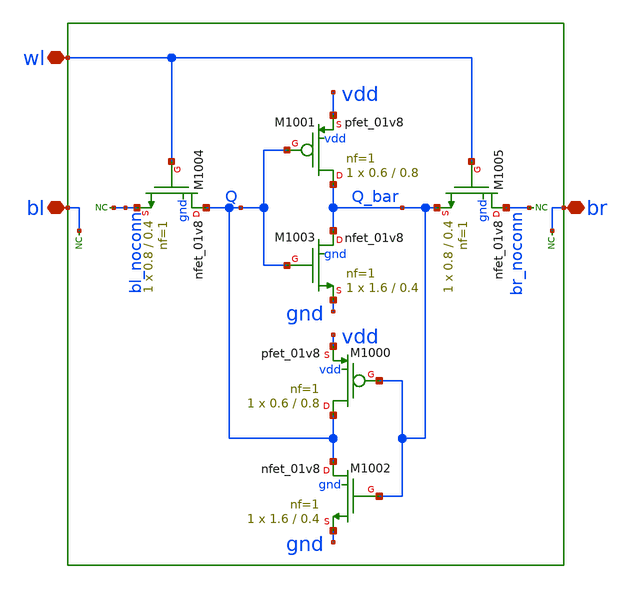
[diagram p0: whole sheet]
** sch_path: sram_2_64_scn4m_lcc/dummy_cell_1rw.sch
**.subckt dummy_cell_1rw bl br wl
*.iopin bl
*.iopin br
*.iopin wl
XM1004 Q wl bl_noconn gnd sky130_fd_pr__nfet_01v8 L=0.4 W=0.8 nf=1 ad='int((nf+1)/2) * W/nf * 0.29' as='int((nf+2)/2) * W/nf * 0.29'
+ pd='2*int((nf+1)/2) * (W/nf + 0.29)' ps='2*int((nf+2)/2) * (W/nf + 0.29)' nrd='0.29 / W' nrs='0.29 / W'
+ sa=0 sb=0 sd=0 mult=1 m=1
XM1001 Q_bar Q vdd vdd sky130_fd_pr__pfet_01v8 L=0.8 W=0.6 nf=1 ad='int((nf+1)/2) * W/nf * 0.29' as='int((nf+2)/2) * W/nf * 0.29'
+ pd='2*int((nf+1)/2) * (W/nf + 0.29)' ps='2*int((nf+2)/2) * (W/nf + 0.29)' nrd='0.29 / W' nrs='0.29 / W'
+ sa=0 sb=0 sd=0 mult=1 m=1
XM1003 Q_bar Q gnd gnd sky130_fd_pr__nfet_01v8 L=0.4 W=1.6 nf=1 ad='int((nf+1)/2) * W/nf * 0.29' as='int((nf+2)/2) * W/nf * 0.29'
+ pd='2*int((nf+1)/2) * (W/nf + 0.29)' ps='2*int((nf+2)/2) * (W/nf + 0.29)' nrd='0.29 / W' nrs='0.29 / W'
+ sa=0 sb=0 sd=0 mult=1 m=1
XM1002 Q Q_bar gnd gnd sky130_fd_pr__nfet_01v8 L=0.4 W=1.6 nf=1 ad='int((nf+1)/2) * W/nf * 0.29' as='int((nf+2)/2) * W/nf * 0.29'
+ pd='2*int((nf+1)/2) * (W/nf + 0.29)' ps='2*int((nf+2)/2) * (W/nf + 0.29)' nrd='0.29 / W' nrs='0.29 / W'
+ sa=0 sb=0 sd=0 mult=1 m=1
XM1000 Q Q_bar vdd vdd sky130_fd_pr__pfet_01v8 L=0.8 W=0.6 nf=1 ad='int((nf+1)/2) * W/nf * 0.29' as='int((nf+2)/2) * W/nf * 0.29'
+ pd='2*int((nf+1)/2) * (W/nf + 0.29)' ps='2*int((nf+2)/2) * (W/nf + 0.29)' nrd='0.29 / W' nrs='0.29 / W'
+ sa=0 sb=0 sd=0 mult=1 m=1
XM1005 br_noconn wl Q_bar gnd sky130_fd_pr__nfet_01v8 L=0.4 W=0.8 nf=1 ad='int((nf+1)/2) * W/nf * 0.29'
+ as='int((nf+2)/2) * W/nf * 0.29' pd='2*int((nf+1)/2) * (W/nf + 0.29)' ps='2*int((nf+2)/2) * (W/nf + 0.29)'
+ nrd='0.29 / W' nrs='0.29 / W' sa=0 sb=0 sd=0 mult=1 m=1
* noconn bl_noconn
* noconn br_noconn
* noconn br
* noconn bl
**.ends
.end
